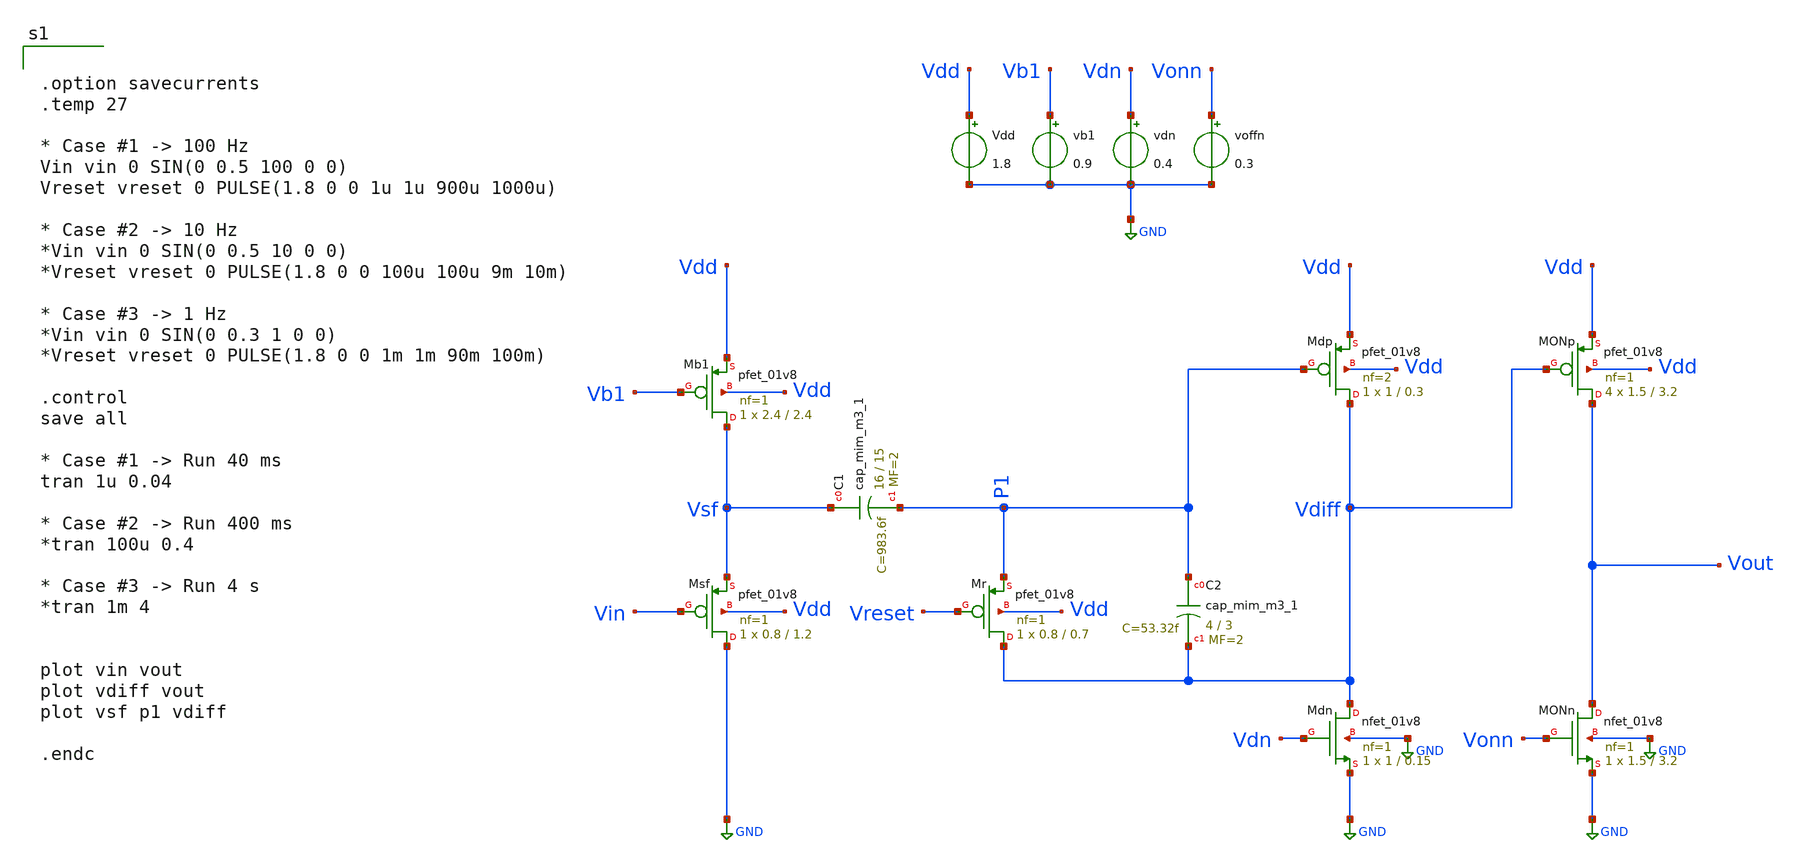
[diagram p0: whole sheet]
** sch_path: Schematic/AFE 2.sch
**.subckt AFE 2
XMsf GND Vin Vsf Vdd sky130_fd_pr__pfet_01v8 L=1.2 W=0.8 nf=1 ad='int((nf+1)/2) * W/nf * 0.29' as='int((nf+2)/2) * W/nf * 0.29'
+ pd='2*int((nf+1)/2) * (W/nf + 0.29)' ps='2*int((nf+2)/2) * (W/nf + 0.29)' nrd='0.29 / W' nrs='0.29 / W'
+ sa=0 sb=0 sd=0 mult=1 m=1
XMb1 Vsf Vb1 Vdd Vdd sky130_fd_pr__pfet_01v8 L=2.4 W=2.4 nf=1 ad='int((nf+1)/2) * W/nf * 0.29' as='int((nf+2)/2) * W/nf * 0.29'
+ pd='2*int((nf+1)/2) * (W/nf + 0.29)' ps='2*int((nf+2)/2) * (W/nf + 0.29)' nrd='0.29 / W' nrs='0.29 / W'
+ sa=0 sb=0 sd=0 mult=1 m=1
XC1 Vsf P1 sky130_fd_pr__cap_mim_m3_1 W=16 L=15 MF=2 m=2
XC2 P1 Vdiff sky130_fd_pr__cap_mim_m3_1 W=4 L=3 MF=2 m=2
XMr Vdiff Vreset P1 Vdd sky130_fd_pr__pfet_01v8 L=0.7 W=0.8 nf=1 ad='int((nf+1)/2) * W/nf * 0.29' as='int((nf+2)/2) * W/nf * 0.29'
+ pd='2*int((nf+1)/2) * (W/nf + 0.29)' ps='2*int((nf+2)/2) * (W/nf + 0.29)' nrd='0.29 / W' nrs='0.29 / W'
+ sa=0 sb=0 sd=0 mult=1 m=1
XMdp Vdiff P1 Vdd Vdd sky130_fd_pr__pfet_01v8 L=0.3 W=1 nf=2 ad='int((nf+1)/2) * W/nf * 0.29' as='int((nf+2)/2) * W/nf * 0.29'
+ pd='2*int((nf+1)/2) * (W/nf + 0.29)' ps='2*int((nf+2)/2) * (W/nf + 0.29)' nrd='0.29 / W' nrs='0.29 / W'
+ sa=0 sb=0 sd=0 mult=1 m=1
XMdn Vdiff Vdn GND GND sky130_fd_pr__nfet_01v8 L=0.15 W=1 nf=1 ad='int((nf+1)/2) * W/nf * 0.29' as='int((nf+2)/2) * W/nf * 0.29'
+ pd='2*int((nf+1)/2) * (W/nf + 0.29)' ps='2*int((nf+2)/2) * (W/nf + 0.29)' nrd='0.29 / W' nrs='0.29 / W'
+ sa=0 sb=0 sd=0 mult=1 m=1
XMONp Vout Vdiff Vdd Vdd sky130_fd_pr__pfet_01v8 L=3.2 W=1.5 nf=1 ad='int((nf+1)/2) * W/nf * 0.29' as='int((nf+2)/2) * W/nf * 0.29'
+ pd='2*int((nf+1)/2) * (W/nf + 0.29)' ps='2*int((nf+2)/2) * (W/nf + 0.29)' nrd='0.29 / W' nrs='0.29 / W'
+ sa=0 sb=0 sd=0 mult=4 m=4
XMONn Vout Vonn GND GND sky130_fd_pr__nfet_01v8 L=3.2 W=1.5 nf=1 ad='int((nf+1)/2) * W/nf * 0.29' as='int((nf+2)/2) * W/nf * 0.29'
+ pd='2*int((nf+1)/2) * (W/nf + 0.29)' ps='2*int((nf+2)/2) * (W/nf + 0.29)' nrd='0.29 / W' nrs='0.29 / W'
+ sa=0 sb=0 sd=0 mult=1 m=1
Vdd Vdd GND 1.8
vb1 Vb1 GND 0.9
vdn Vdn GND 0.4
voffn Vonn GND 0.3
**** begin user architecture code

** opencircuitdesign pdks install
.lib $::SKYWATER_MODELS/sky130.lib.spice tt




.option savecurrents
.temp 27

* Case #1 -> 100 Hz
Vin vin 0 SIN(0 0.5 100 0 0)
Vreset vreset 0 PULSE(1.8 0 0 1u 1u 900u 1000u)

* Case #2 -> 10 Hz
*Vin vin 0 SIN(0 0.5 10 0 0)
*Vreset vreset 0 PULSE(1.8 0 0 100u 100u 9m 10m)

* Case #3 -> 1 Hz
*Vin vin 0 SIN(0 0.3 1 0 0)
*Vreset vreset 0 PULSE(1.8 0 0 1m 1m 90m 100m)

.control
save all

* Case #1 -> Run 40 ms
tran 1u 0.04

* Case #2 -> Run 400 ms
*tran 100u 0.4

* Case #3 -> Run 4 s
*tran 1m 4


plot vin vout
plot vdiff vout
plot vsf p1 vdiff

.endc

**** end user architecture code
**.ends
.GLOBAL GND
.end
